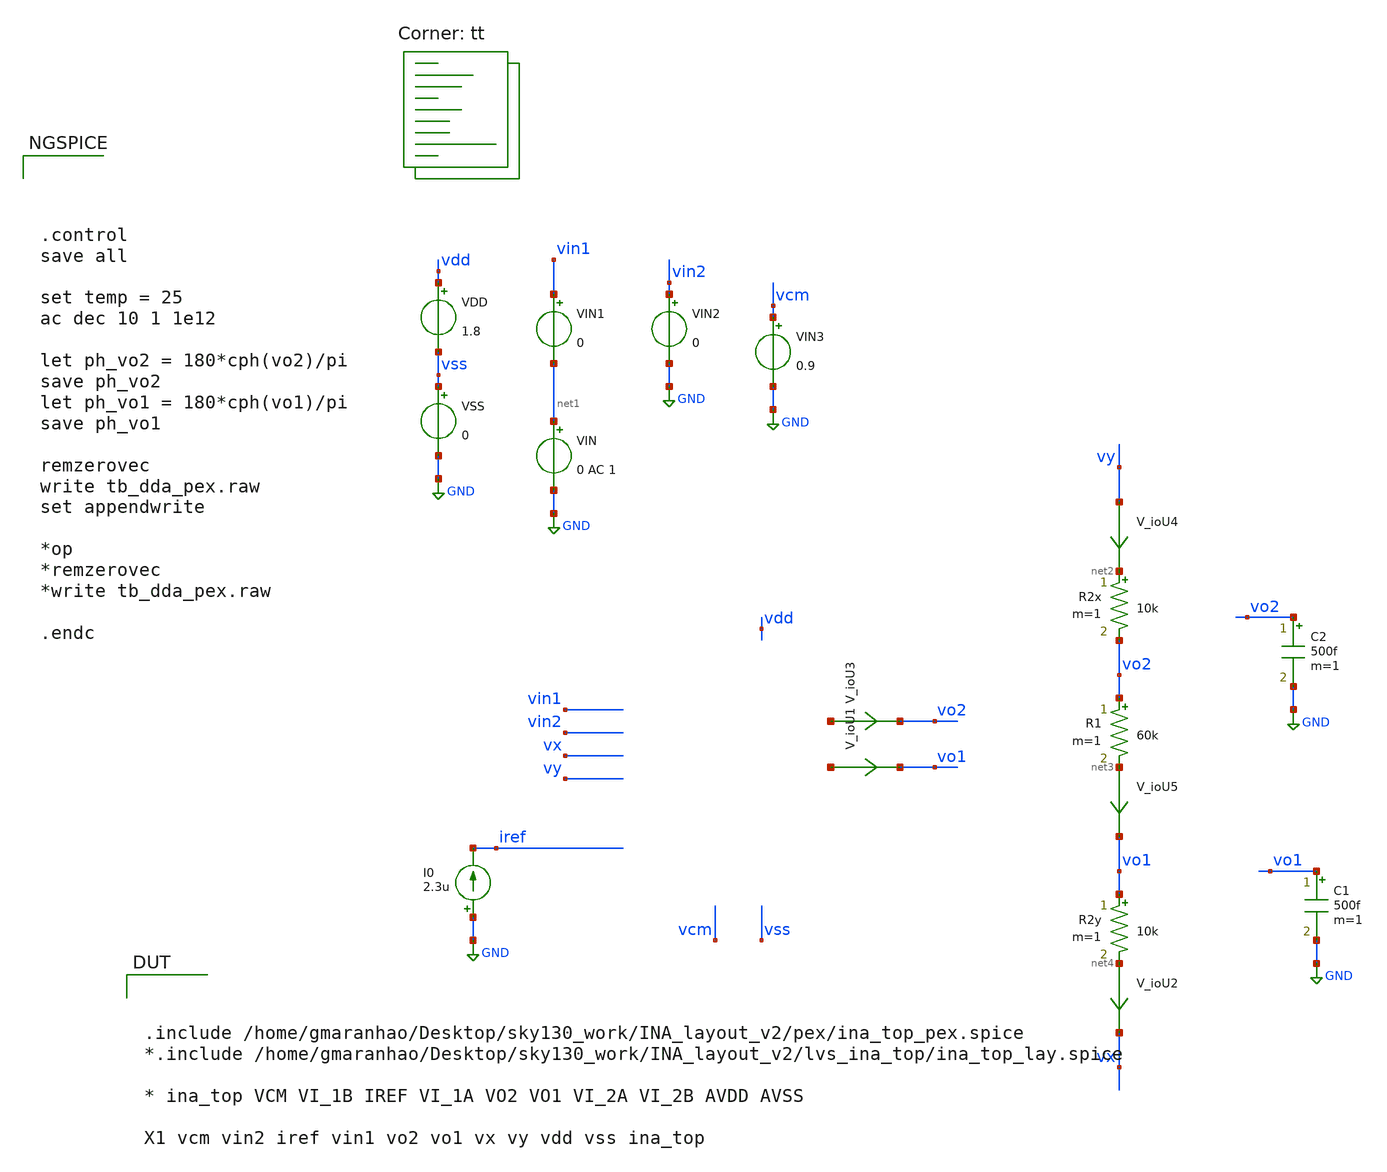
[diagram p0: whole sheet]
** sch_path: testbenches/tb_dda_pex.sch
**.subckt tb_dda_pex
VDD vdd vss 1.8
VSS vss GND 0
C1 vo1 GND 500f m=1
I0 GND iref 2.3u
VIN1 vin1 net1 0
VIN2 vin2 GND 0
VIN net1 GND 0 AC 1
C2 vo2 GND 500f m=1
VIN3 vcm GND 0.9
R2x net2 vo2 10k m=1
R1 vo2 net3 60k m=1
R2y vo1 net4 10k m=1
V_ioU3 net5 vo2 0
.save i(v_iou3)
V_ioU1 net6 vo1 0
.save i(v_iou1)
V_ioU2 net4 vx 0
.save i(v_iou2)
V_ioU4 vy net2 0
.save i(v_iou4)
V_ioU5 net3 vo1 0
.save i(v_iou5)
**** begin user architecture code




.control
save all

set temp = 25
ac dec 10 1 1e12

let ph_vo2 = 180*cph(vo2)/pi
save ph_vo2
let ph_vo1 = 180*cph(vo1)/pi
save ph_vo1

remzerovec
write tb_dda_pex.raw
set appendwrite

*op
*remzerovec
*write tb_dda_pex.raw

.endc


.lib $::SKYWATER_MODELS/sky130.lib.spice tt


.include /home/gmaranhao/Desktop/sky130_work/INA_layout_v2/pex/ina_top_pex.spice
*.include /home/gmaranhao/Desktop/sky130_work/INA_layout_v2/lvs_ina_top/ina_top_lay.spice

* ina_top VCM VI_1B IREF VI_1A VO2 VO1 VI_2A VI_2B AVDD AVSS

X1 vcm vin2 iref vin1 vo2 vo1 vx vy vdd vss ina_top


**** end user architecture code
**.ends
.GLOBAL GND
.end
